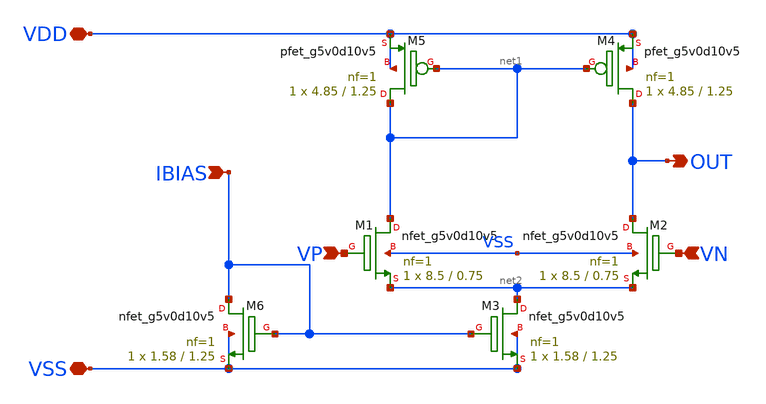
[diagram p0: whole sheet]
** sch_path: xschem/5t-ota/schematics/5t-ota.sch
**.subckt 5t-ota VP VN IBIAS VDD VSS OUT
*.ipin VP
*.ipin VN
*.ipin IBIAS
*.iopin VDD
*.iopin VSS
*.opin OUT
XM1 net1 VP net2 VSS sky130_fd_pr__nfet_g5v0d10v5 L=0.75 W=8.5 nf=1 ad='int((nf+1)/2) * W/nf * 0.29'
+ as='int((nf+2)/2) * W/nf * 0.29' pd='2*int((nf+1)/2) * (W/nf + 0.29)' ps='2*int((nf+2)/2) * (W/nf + 0.29)'
+ nrd='0.29 / W' nrs='0.29 / W' sa=0 sb=0 sd=0 mult=1 m=1
XM2 OUT VN net2 VSS sky130_fd_pr__nfet_g5v0d10v5 L=0.75 W=8.5 nf=1 ad='int((nf+1)/2) * W/nf * 0.29' as='int((nf+2)/2) * W/nf * 0.29'
+ pd='2*int((nf+1)/2) * (W/nf + 0.29)' ps='2*int((nf+2)/2) * (W/nf + 0.29)' nrd='0.29 / W' nrs='0.29 / W'
+ sa=0 sb=0 sd=0 mult=1 m=1
XM3 net2 IBIAS VSS VSS sky130_fd_pr__nfet_g5v0d10v5 L=1.25 W=1.58 nf=1 ad='int((nf+1)/2) * W/nf * 0.29'
+ as='int((nf+2)/2) * W/nf * 0.29' pd='2*int((nf+1)/2) * (W/nf + 0.29)' ps='2*int((nf+2)/2) * (W/nf + 0.29)'
+ nrd='0.29 / W' nrs='0.29 / W' sa=0 sb=0 sd=0 mult=1 m=1
XM4 OUT net1 VDD VDD sky130_fd_pr__pfet_g5v0d10v5 L=1.25 W=4.85 nf=1 ad='int((nf+1)/2) * W/nf * 0.29'
+ as='int((nf+2)/2) * W/nf * 0.29' pd='2*int((nf+1)/2) * (W/nf + 0.29)' ps='2*int((nf+2)/2) * (W/nf + 0.29)'
+ nrd='0.29 / W' nrs='0.29 / W' sa=0 sb=0 sd=0 mult=1 m=1
XM5 net1 net1 VDD VDD sky130_fd_pr__pfet_g5v0d10v5 L=1.25 W=4.85 nf=1 ad='int((nf+1)/2) * W/nf * 0.29'
+ as='int((nf+2)/2) * W/nf * 0.29' pd='2*int((nf+1)/2) * (W/nf + 0.29)' ps='2*int((nf+2)/2) * (W/nf + 0.29)'
+ nrd='0.29 / W' nrs='0.29 / W' sa=0 sb=0 sd=0 mult=1 m=1
XM6 IBIAS IBIAS VSS VSS sky130_fd_pr__nfet_g5v0d10v5 L=1.25 W=1.58 nf=1 ad='int((nf+1)/2) * W/nf * 0.29'
+ as='int((nf+2)/2) * W/nf * 0.29' pd='2*int((nf+1)/2) * (W/nf + 0.29)' ps='2*int((nf+2)/2) * (W/nf + 0.29)'
+ nrd='0.29 / W' nrs='0.29 / W' sa=0 sb=0 sd=0 mult=1 m=1
**.ends
.end
